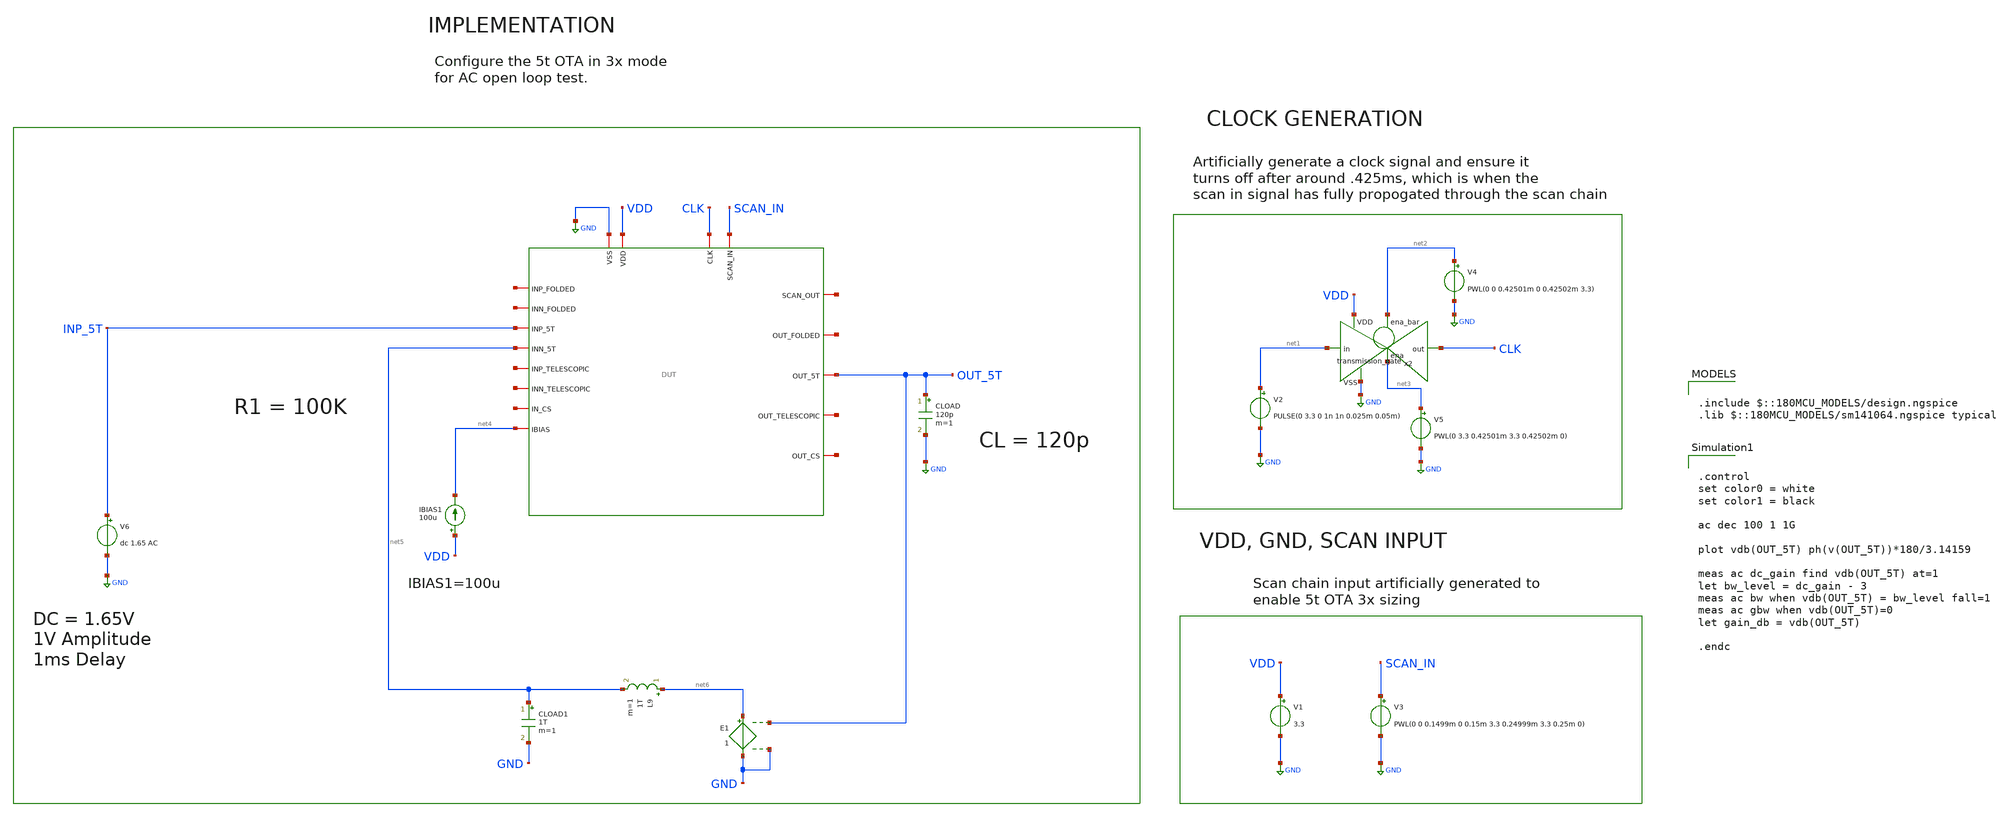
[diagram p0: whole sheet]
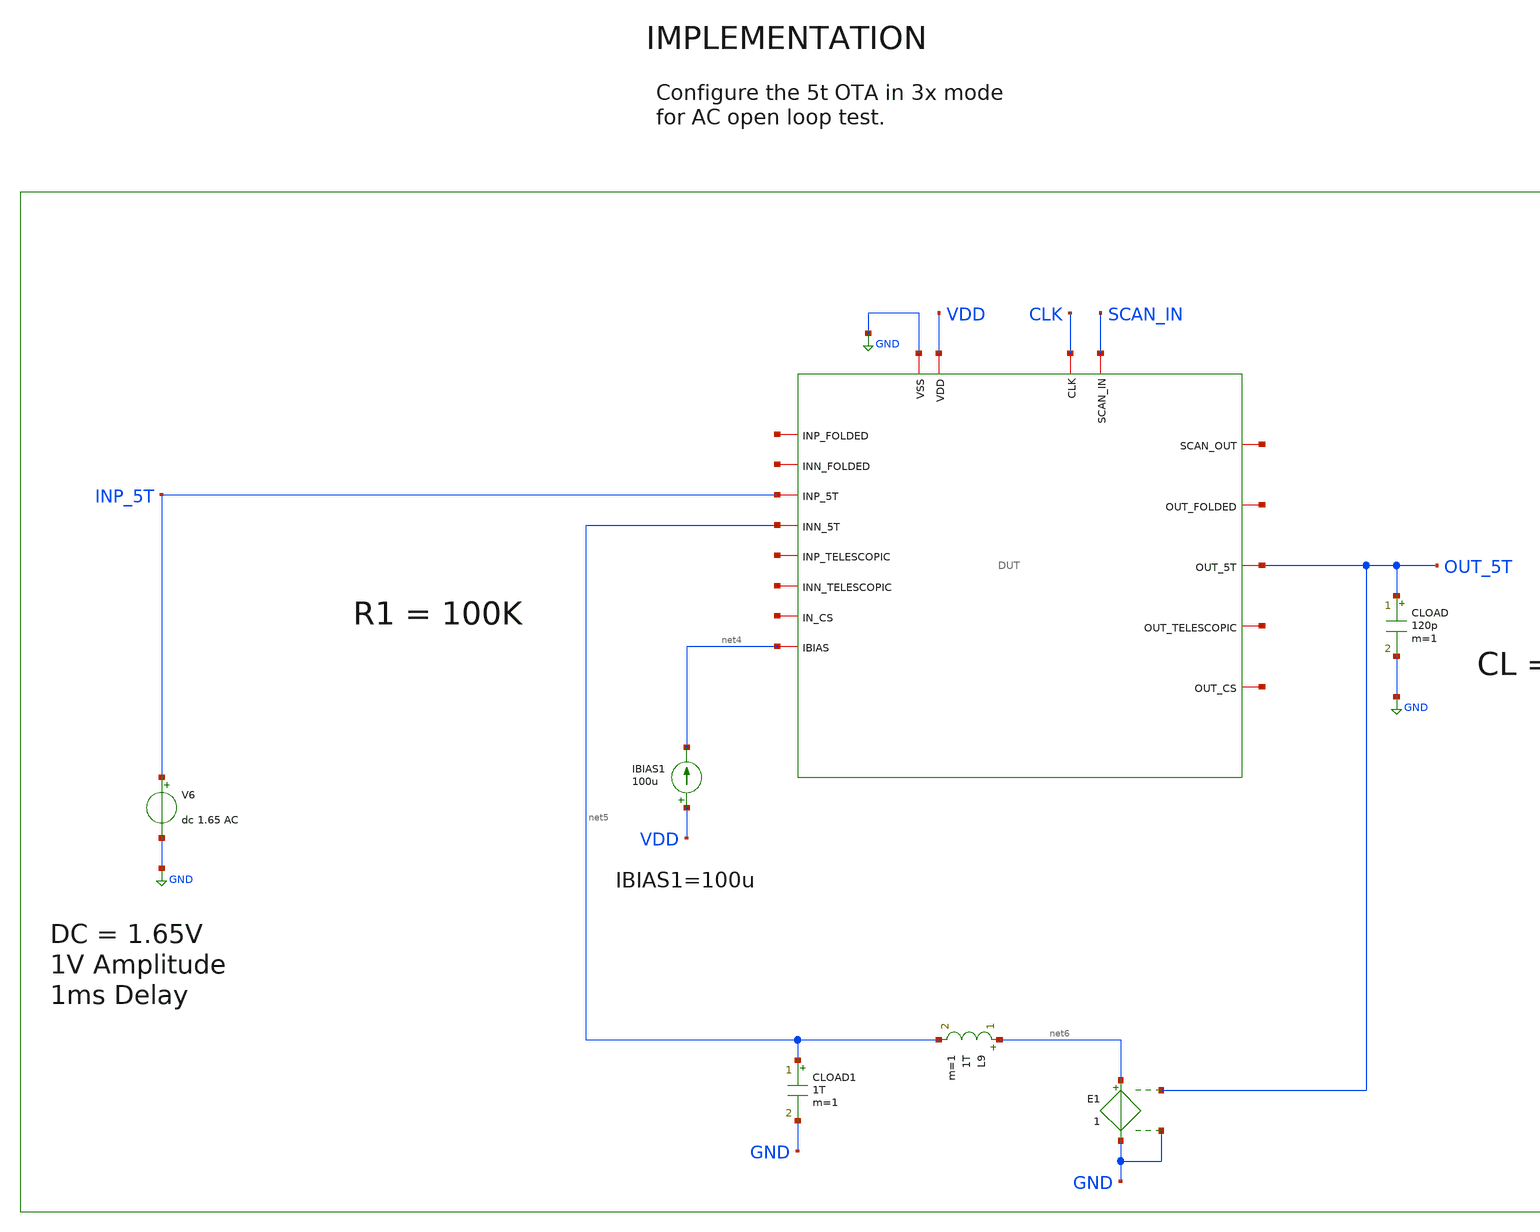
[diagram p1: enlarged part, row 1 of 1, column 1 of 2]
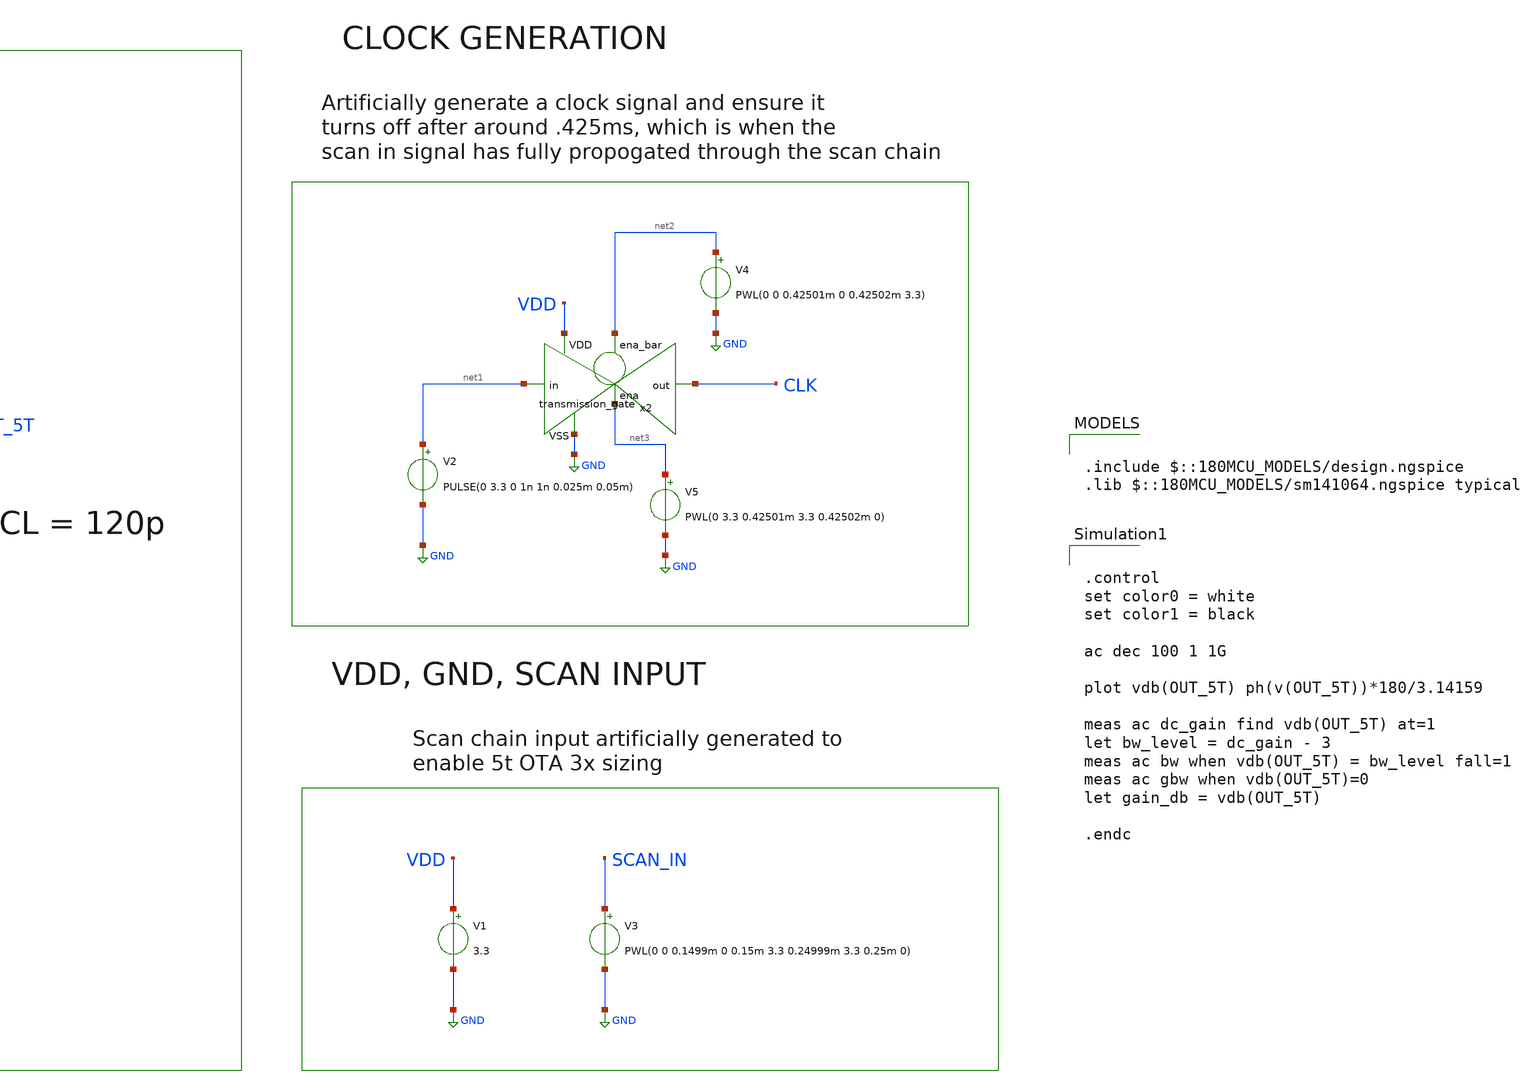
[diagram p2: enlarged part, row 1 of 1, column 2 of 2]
** sch_path: designs/libs/core_tb/sl/ota_5t/5t_tran_ac_open_loop_3x.sch
**.subckt 5t_tran_ac_open_loop_3x
V3 SCAN_IN GND PWL(0 0 0.1499m 0 0.15m 3.3 0.24999m 3.3 0.25m 0)
V1 VDD GND 3.3
V2 net1 GND PULSE(0 3.3 0 1n 1n 0.025m 0.05m)
x2 net2 VDD CLK net1 GND net3 transmission_gate
V4 net2 GND PWL(0 0 0.42501m 0 0.42502m 3.3)
V5 net3 GND PWL(0 3.3 0.42501m 3.3 0.42502m 0)
IBIAS1 VDD net4 100u
CLOAD OUT_5T GND 120p m=1
V6 INP_5T GND dc 1.65 AC
x1 CLK net7 SCAN_IN GND VDD net8 net9 OUT_5T net4 net10 INP_5T net5 net11 net12 net13 net14 net15
+ DUT
L9 net6 net5 1T m=1
CLOAD1 net5 GND 1T m=1
E1 net6 GND OUT_5T GND 1
**** begin user architecture code

.include $::180MCU_MODELS/design.ngspice
.lib $::180MCU_MODELS/sm141064.ngspice typical



.control
set color0 = white
set color1 = black

ac dec 100 1 1G

plot vdb(OUT_5T) ph(v(OUT_5T))*180/3.14159

meas ac dc_gain find vdb(OUT_5T) at=1
let bw_level = dc_gain - 3
meas ac bw when vdb(OUT_5T) = bw_level fall=1
meas ac gbw when vdb(OUT_5T)=0
let gain_db = vdb(OUT_5T)

.endc


**** end user architecture code
**.ends
.GLOBAL GND
.end
